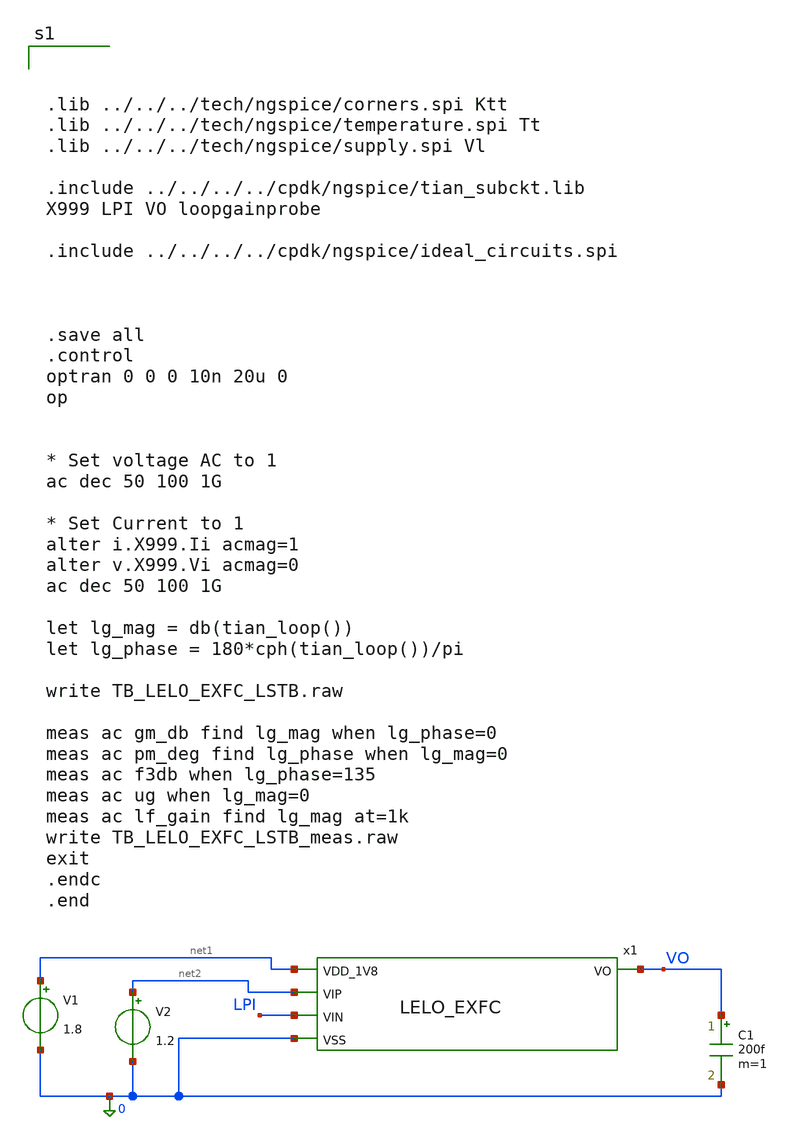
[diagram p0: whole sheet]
** sch_path: design/LELO_EXFC_SKY130A/TB_LELO_EXFC_LSTB.sch
**.subckt TB_LELO_EXFC_LSTB
x1 net1 VO net2 LPI 0 LELO_EXFC
V1 net1 0 1.8
V2 net2 0 1.2
C1 VO 0 200f m=1
**** begin user architecture code



.lib ../../../tech/ngspice/corners.spi Ktt
.lib ../../../tech/ngspice/temperature.spi Tt
.lib ../../../tech/ngspice/supply.spi Vl

.include ../../../../cpdk/ngspice/tian_subckt.lib
X999 LPI VO loopgainprobe

.include ../../../../cpdk/ngspice/ideal_circuits.spi



.save all
.control
optran 0 0 0 10n 20u 0
op


* Set voltage AC to 1
ac dec 50 100 1G

* Set Current to 1
alter i.X999.Ii acmag=1
alter v.X999.Vi acmag=0
ac dec 50 100 1G

let lg_mag = db(tian_loop())
let lg_phase = 180*cph(tian_loop())/pi

write TB_LELO_EXFC_LSTB.raw

meas ac gm_db find lg_mag when lg_phase=0
meas ac pm_deg find lg_phase when lg_mag=0
meas ac f3db when lg_phase=135
meas ac ug when lg_mag=0
meas ac lf_gain find lg_mag at=1k
write TB_LELO_EXFC_LSTB_meas.raw
exit
.endc
.end



**** end user architecture code
**.ends
.end
